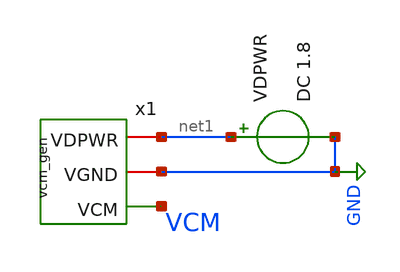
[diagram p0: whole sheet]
** sch_path: xschem/tb_vcm_gen.sch
**.subckt tb_vcm_gen
x1 net1 GND VCM vcm_gen
VDPWR net1 GND DC 1.8
**** begin user architecture code


.lib /foss/pdks/sky130A/libs.tech/ngspice/sky130.lib.spice tt_mm

.option savecurrents

.control

op

print v(vcm)

tran 100u 20m

plot v(vcm)

.endc


**** end user architecture code
**.ends

* expanding   symbol:  vcm_gen.sym # of pins=3
** sym_path: xschem/vcm_gen.sym
** sch_path: xschem/vcm_gen.sch
.subckt vcm_gen VDPWR VGND VCM
*.iopin VGND
*.iopin VDPWR
*.opin VCM
XC_VCM VGND VCM sky130_fd_pr__cap_mim_m3_1 W=25 L=25 MF=1 m=1
XR_VCM_TOP VCM VDPWR VGND sky130_fd_pr__res_xhigh_po_0p35 L=175 mult=1 m=1
XR_VCM_BOTTOM VGND VCM VGND sky130_fd_pr__res_xhigh_po_0p35 L=175 mult=1 m=1
.ends

.GLOBAL GND
.end
